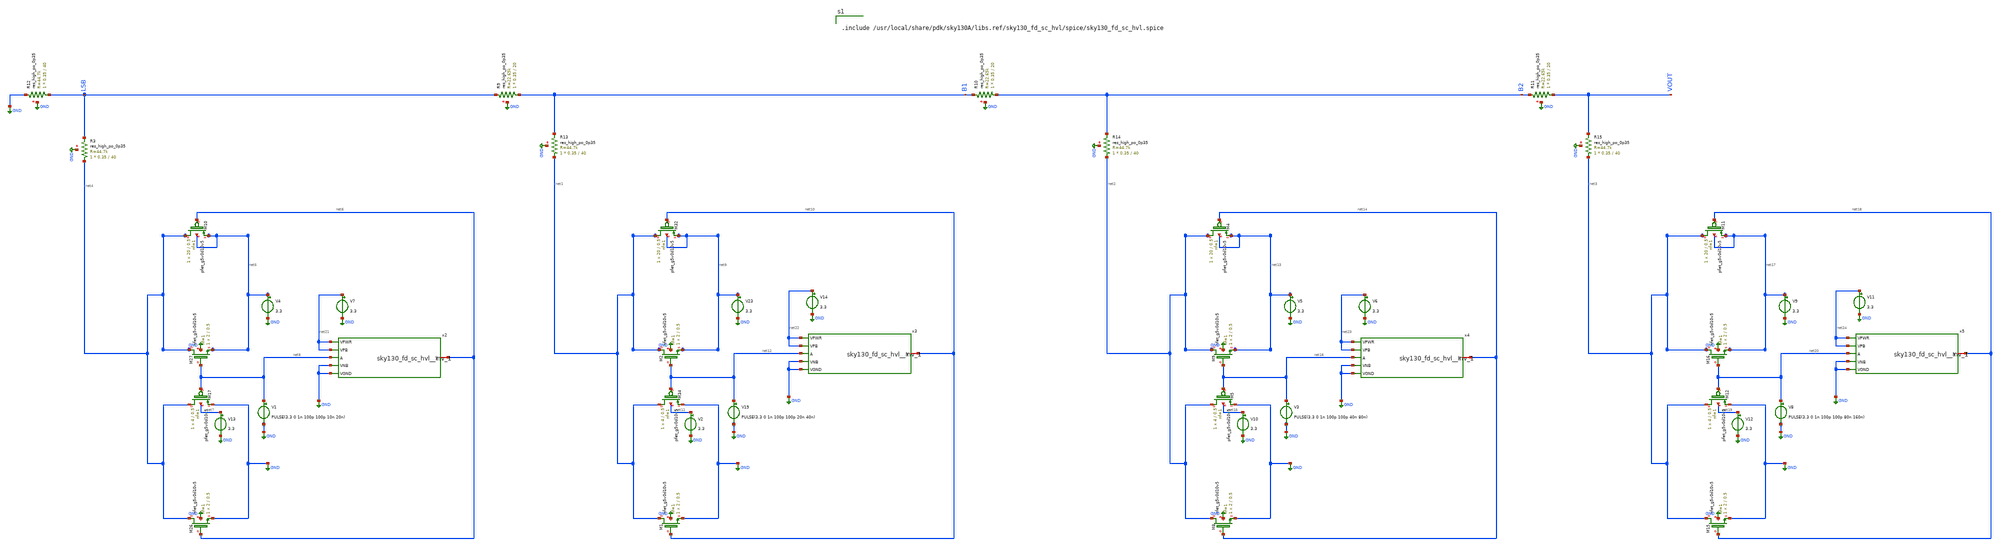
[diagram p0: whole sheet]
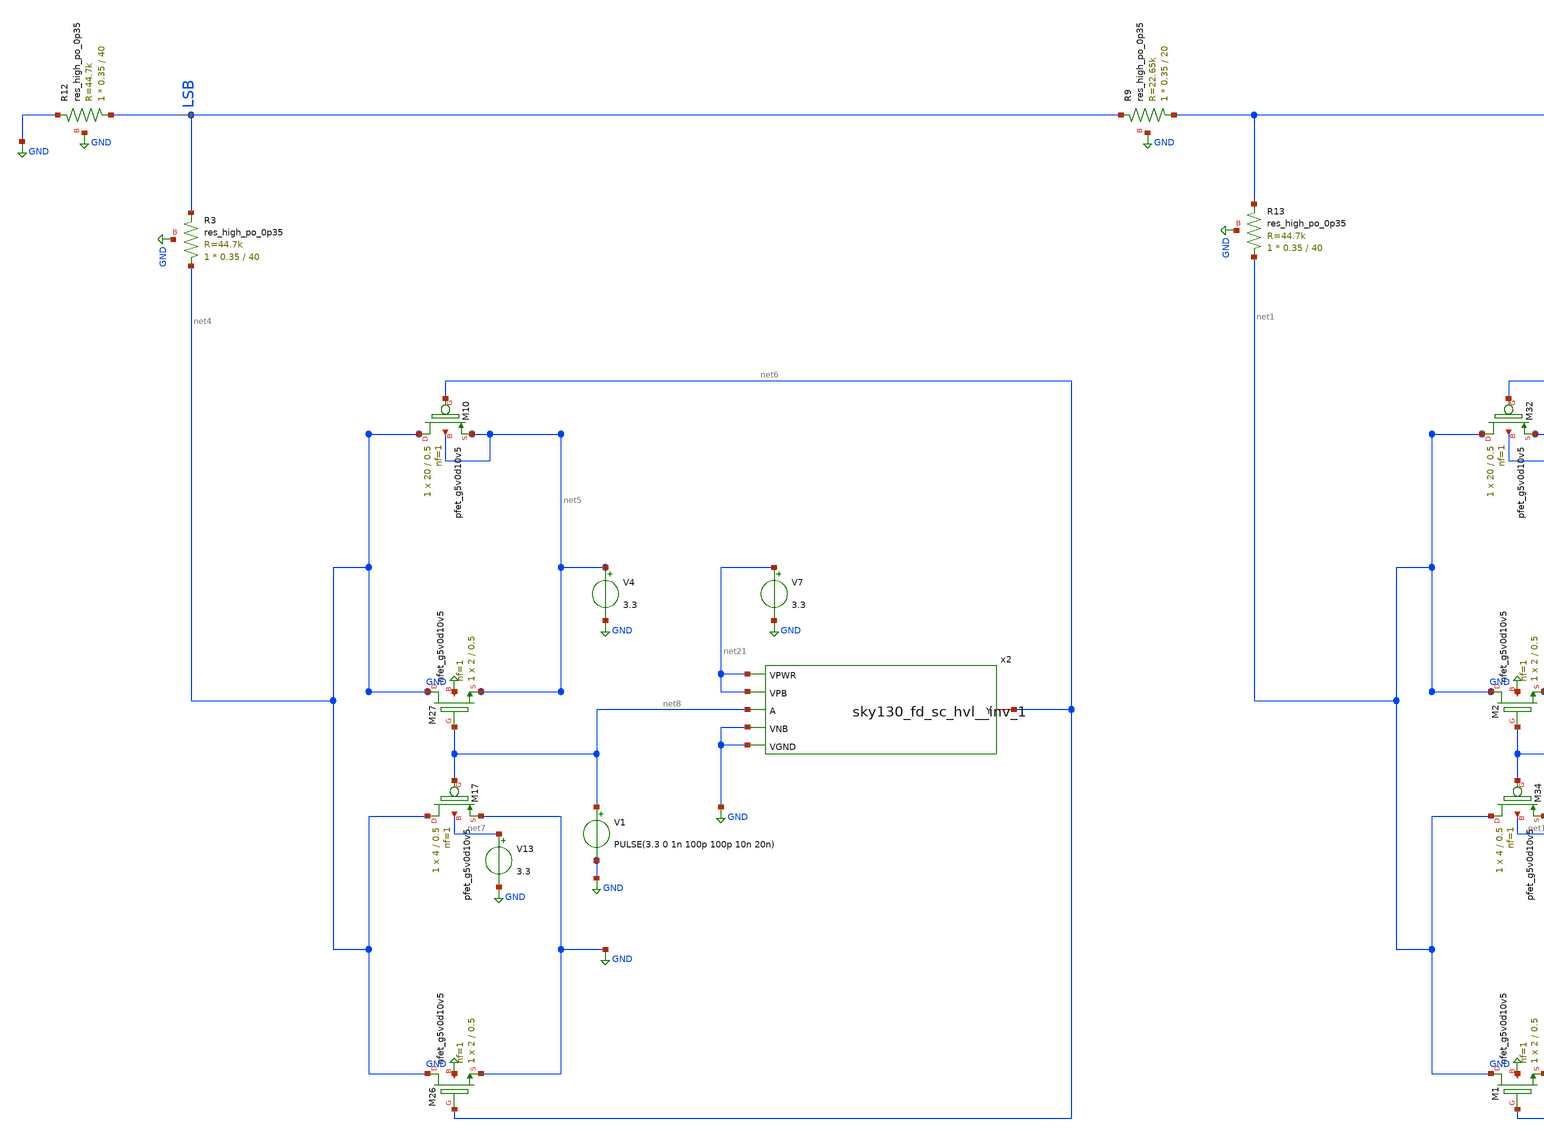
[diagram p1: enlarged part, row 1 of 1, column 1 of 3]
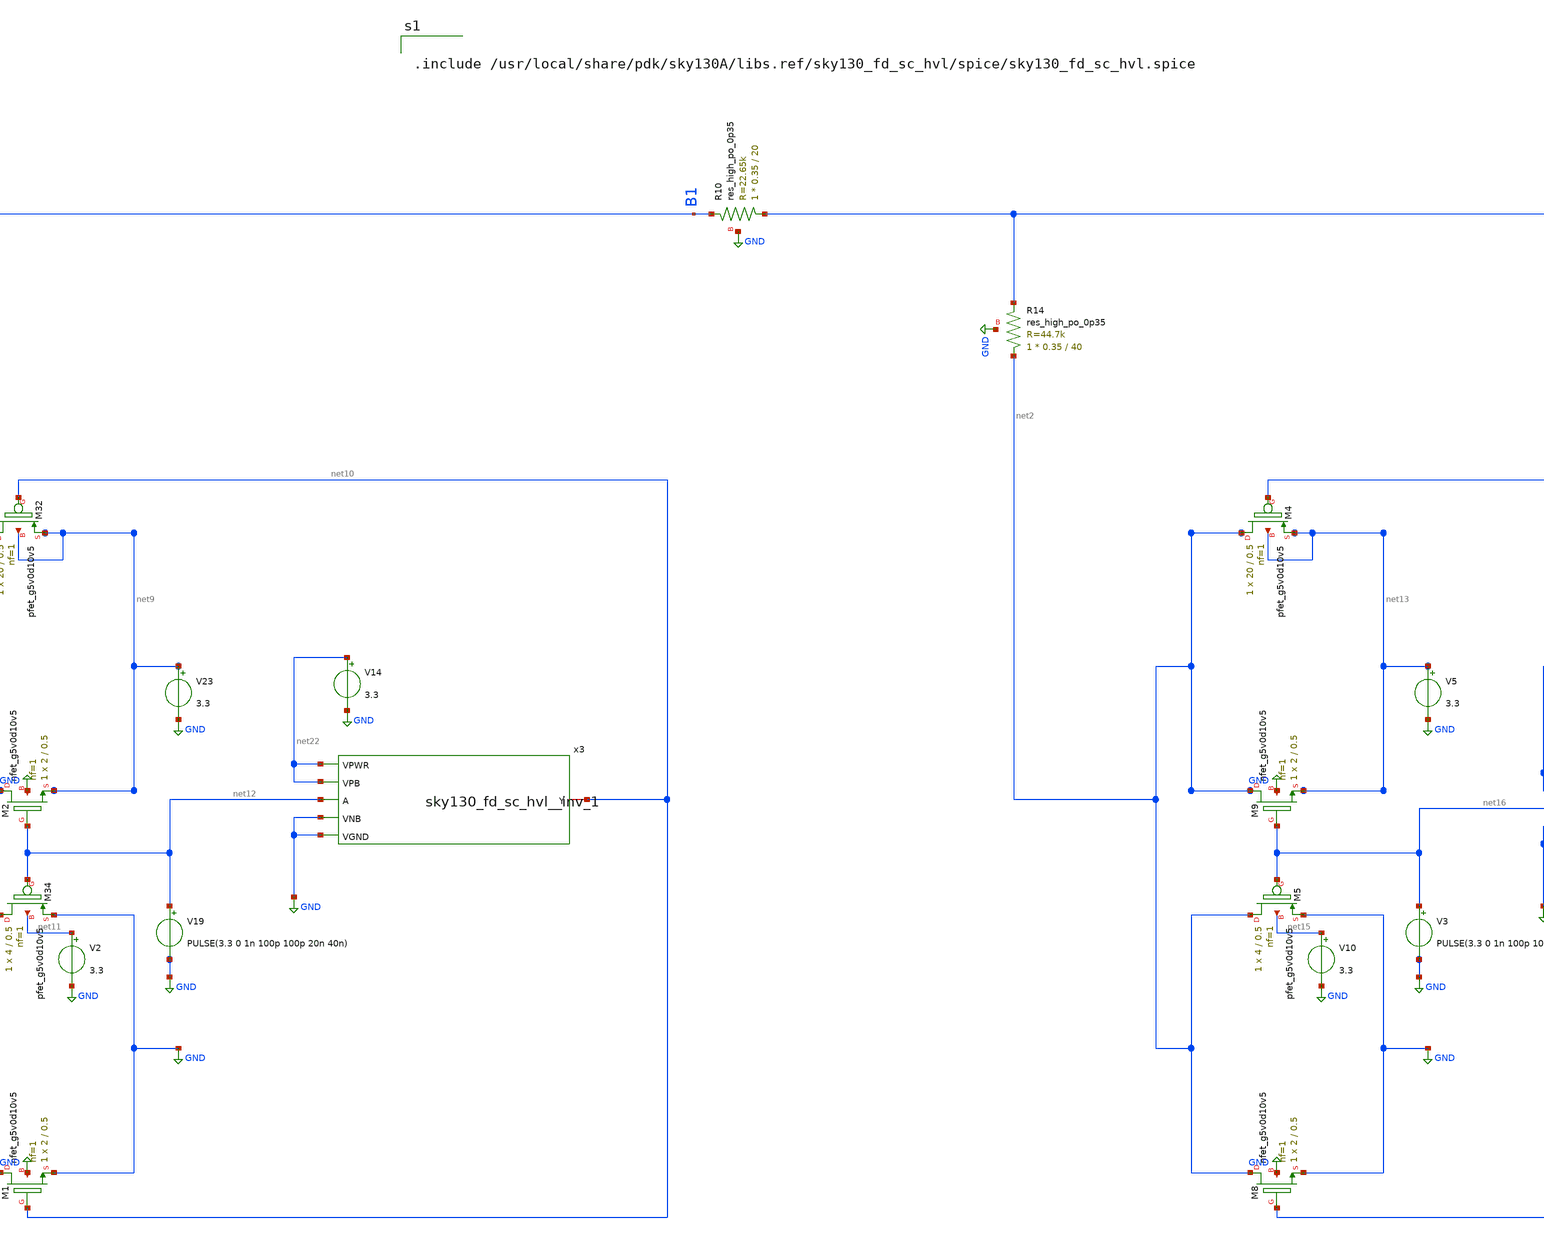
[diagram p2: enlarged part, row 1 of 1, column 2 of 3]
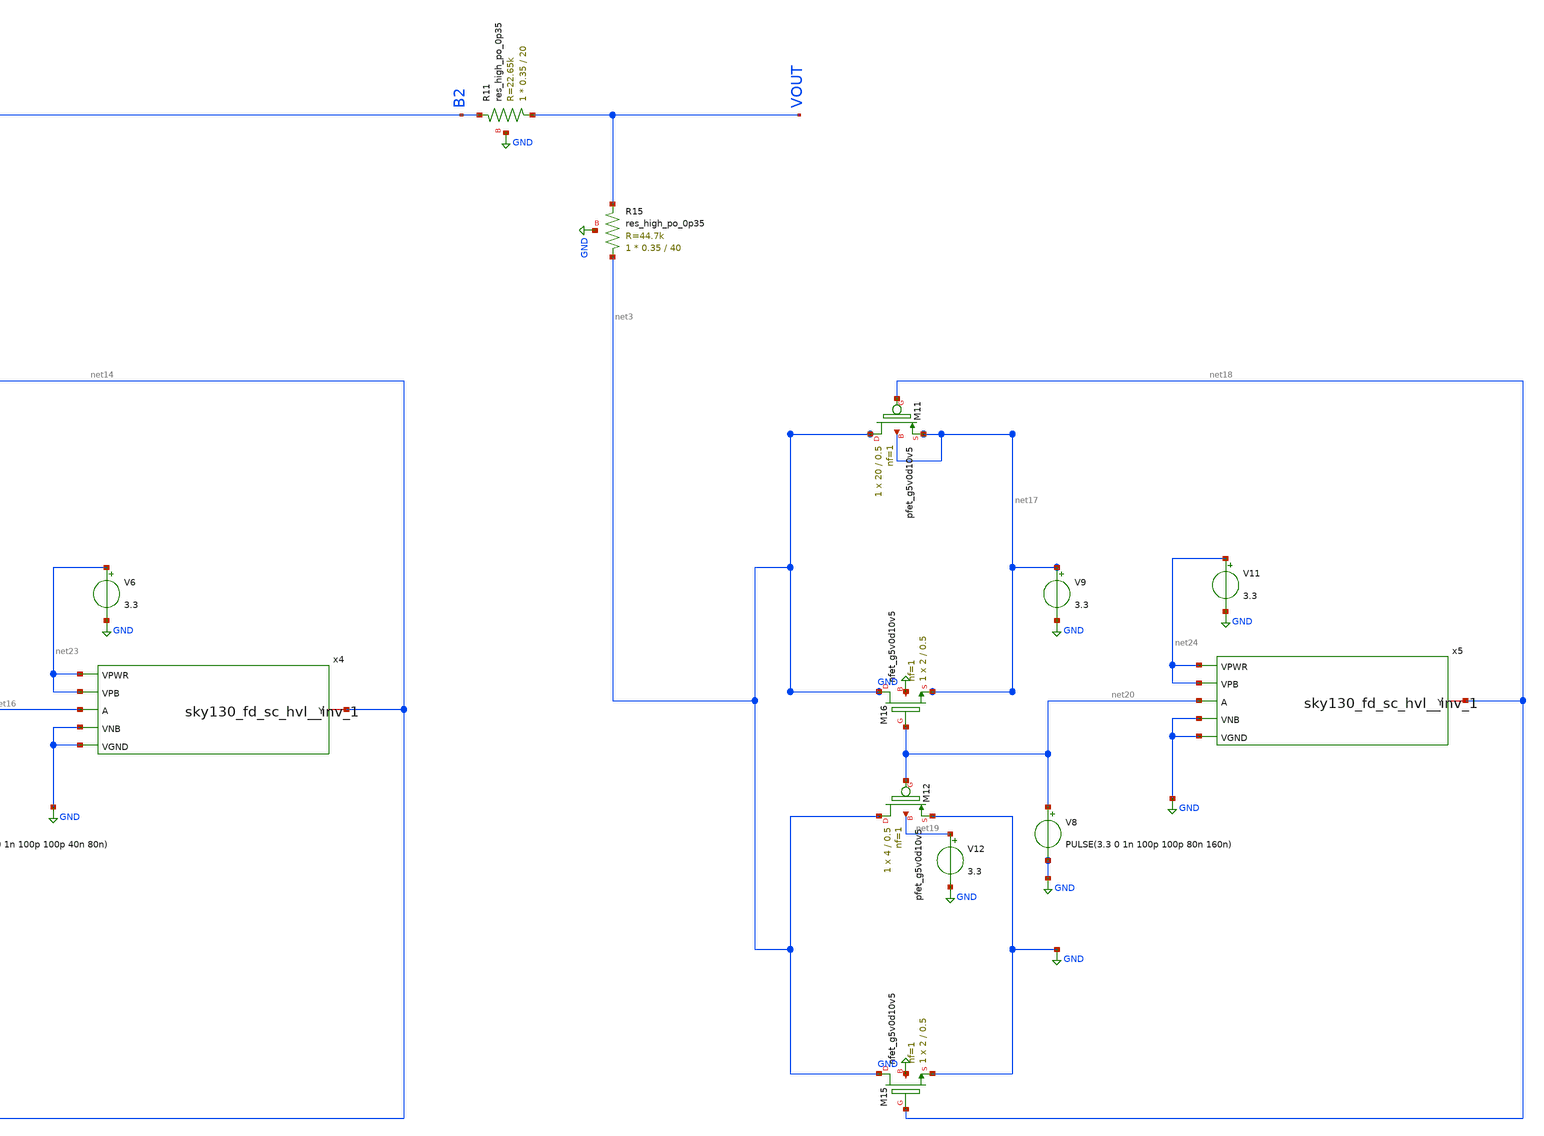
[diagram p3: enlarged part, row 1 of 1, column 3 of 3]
** sch_path: xschem/dac_sim_tb.sch
**.subckt dac_sim_tb
V1 net8 GND PULSE(3.3 0 1n 100p 100p 10n 20n)
XM10 net4 net6 net5 net5 sky130_fd_pr__pfet_g5v0d10v5 L=0.5 W=20 nf=1 ad=0 as=0 pd=0 ps=0 nrd=0
+ nrs=0 sa=0 sb=0 sd=0 mult=1 m=1
V4 net5 GND 3.3
XM17 net4 net8 GND net7 sky130_fd_pr__pfet_g5v0d10v5 L=0.5 W=4 nf=1 ad=0 as=0 pd=0 ps=0 nrd=0 nrs=0
+ sa=0 sb=0 sd=0 mult=1 m=1
XM26 net4 net6 GND GND sky130_fd_pr__nfet_g5v0d10v5 L=0.5 W=2 nf=1 ad=0 as=0 pd=0 ps=0 nrd=0 nrs=0
+ sa=0 sb=0 sd=0 mult=1 m=1
XM27 net4 net8 net5 GND sky130_fd_pr__nfet_g5v0d10v5 L=0.5 W=2 nf=1 ad=0 as=0 pd=0 ps=0 nrd=0 nrs=0
+ sa=0 sb=0 sd=0 mult=1 m=1
V13 net7 GND 3.3
V19 net12 GND PULSE(3.3 0 1n 100p 100p 20n 40n)
XM32 net1 net10 net9 net9 sky130_fd_pr__pfet_g5v0d10v5 L=0.5 W=20 nf=1 ad=0 as=0 pd=0 ps=0 nrd=0
+ nrs=0 sa=0 sb=0 sd=0 mult=1 m=1
V23 net9 GND 3.3
XM34 net1 net12 GND net11 sky130_fd_pr__pfet_g5v0d10v5 L=0.5 W=4 nf=1 ad=0 as=0 pd=0 ps=0 nrd=0
+ nrs=0 sa=0 sb=0 sd=0 mult=1 m=1
XM1 net1 net10 GND GND sky130_fd_pr__nfet_g5v0d10v5 L=0.5 W=2 nf=1 ad=0 as=0 pd=0 ps=0 nrd=0 nrs=0
+ sa=0 sb=0 sd=0 mult=1 m=1
XM2 net1 net12 net9 GND sky130_fd_pr__nfet_g5v0d10v5 L=0.5 W=2 nf=1 ad=0 as=0 pd=0 ps=0 nrd=0 nrs=0
+ sa=0 sb=0 sd=0 mult=1 m=1
V2 net11 GND 3.3
V3 net16 GND PULSE(3.3 0 1n 100p 100p 40n 80n)
XM4 net2 net14 net13 net13 sky130_fd_pr__pfet_g5v0d10v5 L=0.5 W=20 nf=1 ad=0 as=0 pd=0 ps=0 nrd=0
+ nrs=0 sa=0 sb=0 sd=0 mult=1 m=1
V5 net13 GND 3.3
XM5 net2 net16 GND net15 sky130_fd_pr__pfet_g5v0d10v5 L=0.5 W=4 nf=1 ad=0 as=0 pd=0 ps=0 nrd=0 nrs=0
+ sa=0 sb=0 sd=0 mult=1 m=1
XM8 net2 net14 GND GND sky130_fd_pr__nfet_g5v0d10v5 L=0.5 W=2 nf=1 ad=0 as=0 pd=0 ps=0 nrd=0 nrs=0
+ sa=0 sb=0 sd=0 mult=1 m=1
XM9 net2 net16 net13 GND sky130_fd_pr__nfet_g5v0d10v5 L=0.5 W=2 nf=1 ad=0 as=0 pd=0 ps=0 nrd=0 nrs=0
+ sa=0 sb=0 sd=0 mult=1 m=1
V10 net15 GND 3.3
V8 net20 GND PULSE(3.3 0 1n 100p 100p 80n 160n)
XM11 net3 net18 net17 net17 sky130_fd_pr__pfet_g5v0d10v5 L=0.5 W=20 nf=1 ad=0 as=0 pd=0 ps=0 nrd=0
+ nrs=0 sa=0 sb=0 sd=0 mult=1 m=1
V9 net17 GND 3.3
XM12 net3 net20 GND net19 sky130_fd_pr__pfet_g5v0d10v5 L=0.5 W=4 nf=1 ad=0 as=0 pd=0 ps=0 nrd=0
+ nrs=0 sa=0 sb=0 sd=0 mult=1 m=1
XM15 net3 net18 GND GND sky130_fd_pr__nfet_g5v0d10v5 L=0.5 W=2 nf=1 ad=0 as=0 pd=0 ps=0 nrd=0 nrs=0
+ sa=0 sb=0 sd=0 mult=1 m=1
XM16 net3 net20 net17 GND sky130_fd_pr__nfet_g5v0d10v5 L=0.5 W=2 nf=1 ad=0 as=0 pd=0 ps=0 nrd=0
+ nrs=0 sa=0 sb=0 sd=0 mult=1 m=1
V12 net19 GND 3.3
XR10 B2 B1 GND sky130_fd_pr__res_high_po_0p35 L=20 mult=1 m=1
XR9 B1 LSB GND sky130_fd_pr__res_high_po_0p35 L=20 mult=1 m=1
XR11 VOUT B2 GND sky130_fd_pr__res_high_po_0p35 L=20 mult=1 m=1
XR12 LSB GND GND sky130_fd_pr__res_high_po_0p35 L=40 mult=1 m=1
XR13 net1 B1 GND sky130_fd_pr__res_high_po_0p35 L=40 mult=1 m=1
XR14 net2 B2 GND sky130_fd_pr__res_high_po_0p35 L=40 mult=1 m=1
XR15 net3 VOUT GND sky130_fd_pr__res_high_po_0p35 L=40 mult=1 m=1
XR3 net4 LSB GND sky130_fd_pr__res_high_po_0p35 L=40 mult=1 m=1
x2 net8 GND GND net21 net21 net6 sky130_fd_sc_hvl__inv_1
V7 net21 GND 3.3
x3 net12 GND GND net22 net22 net10 sky130_fd_sc_hvl__inv_1
V14 net22 GND 3.3
x4 net16 GND GND net23 net23 net14 sky130_fd_sc_hvl__inv_1
V6 net23 GND 3.3
x5 net20 GND GND net24 net24 net18 sky130_fd_sc_hvl__inv_1
V11 net24 GND 3.3
**** begin user architecture code


.lib /usr/local/share/pdk/sky130A/libs.tech/ngspice/sky130.lib.spice tt

.tran 100p 180n 5n
.save all

.control
run
plot v(vout) v(LSB) v(b1) v(b2)
.endc




.include /usr/local/share/pdk/sky130A/libs.ref/sky130_fd_sc_hvl/spice/sky130_fd_sc_hvl.spice


**** end user architecture code
**.ends
.GLOBAL GND
.end
